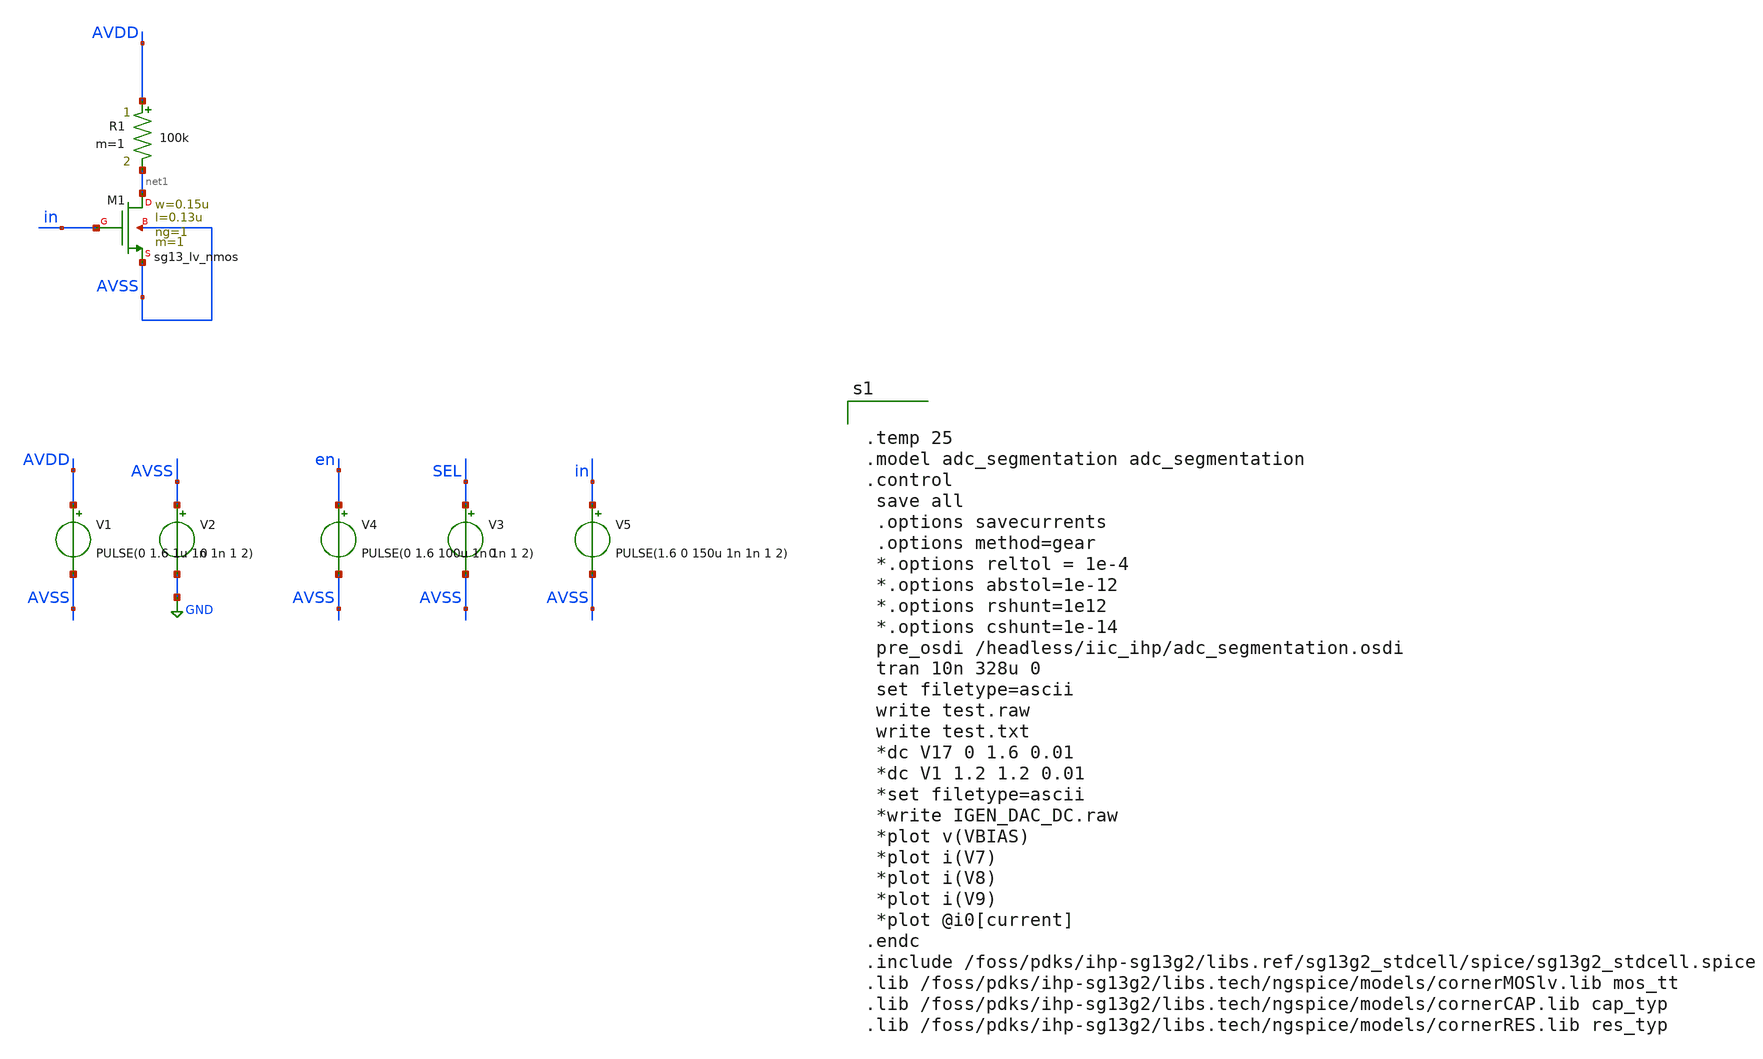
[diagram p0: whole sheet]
** sch_path: current_generator/analog/DAC/schematics/test.sch
**.subckt test
V2 AVSS GND 0
V3 SEL AVSS 0
V4 en AVSS PULSE(0 1.6 100u 1n 1n 1 2)
V5 in AVSS PULSE(1.6 0 150u 1n 1n 1 2)
V1 AVDD AVSS PULSE(0 1.6 1u 1n 1n 1 2)
XM1 net1 in AVSS AVSS sg13_lv_nmos w=0.15u l=0.13u ng=1 m=1 mm_ok=1
R1 AVDD net1 100k m=1
**** begin user architecture code


.temp 25
.model adc_segmentation adc_segmentation
.control
 save all
 .options savecurrents
 .options method=gear
 *.options reltol = 1e-4
 *.options abstol=1e-12
 *.options rshunt=1e12
 *.options cshunt=1e-14
 pre_osdi /headless/iic_ihp/adc_segmentation.osdi
 tran 10n 328u 0
 set filetype=ascii
 write test.raw
 write test.txt
 *dc V17 0 1.6 0.01
 *dc V1 1.2 1.2 0.01
 *set filetype=ascii
 *write IGEN_DAC_DC.raw
 *plot v(VBIAS)
 *plot i(V7)
 *plot i(V8)
 *plot i(V9)
 *plot @i0[current]
.endc
.include /foss/pdks/ihp-sg13g2/libs.ref/sg13g2_stdcell/spice/sg13g2_stdcell.spice
.lib /foss/pdks/ihp-sg13g2/libs.tech/ngspice/models/cornerMOSlv.lib mos_tt
.lib /foss/pdks/ihp-sg13g2/libs.tech/ngspice/models/cornerCAP.lib cap_typ
.lib /foss/pdks/ihp-sg13g2/libs.tech/ngspice/models/cornerRES.lib res_typ


**** end user architecture code
**.ends
.GLOBAL GND
.end
